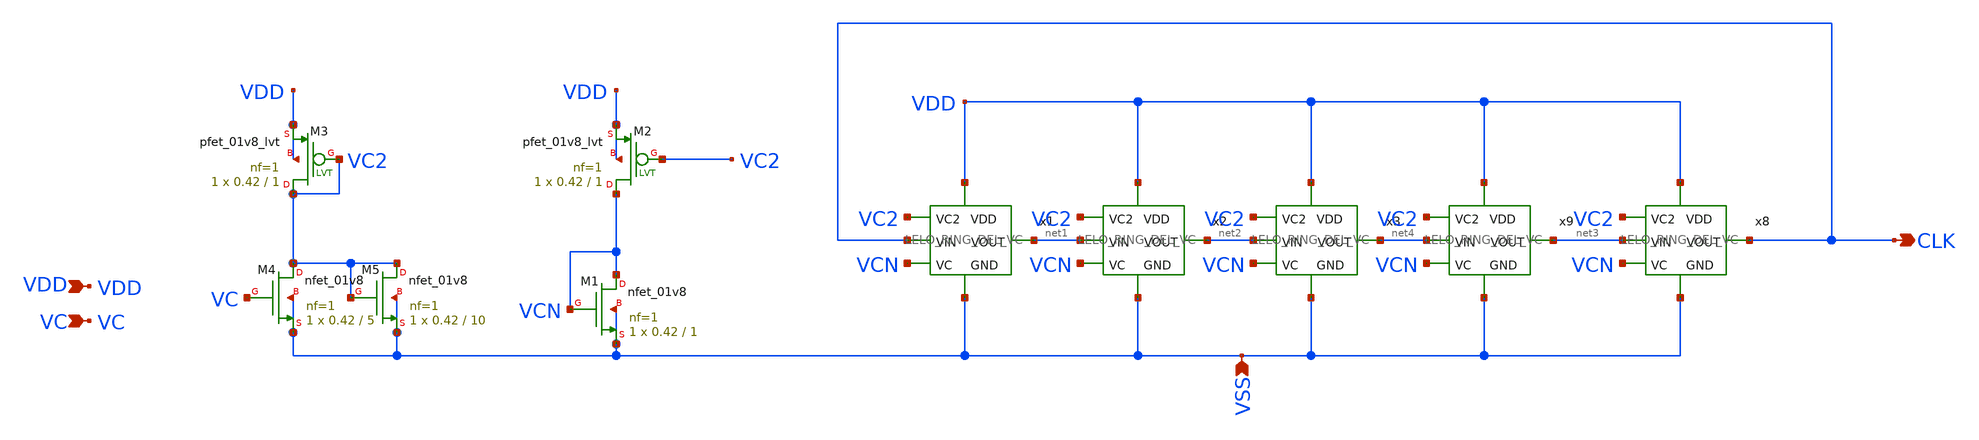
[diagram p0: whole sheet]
** sch_path: design/LELO_SVOD_SKY130A/RO.sch
**.subckt RO CLK VSS VDD VC
*.opin CLK
*.ipin VSS
*.ipin VDD
*.ipin VC
x1 VDD VC2 CLK net1 VCN VSS LELO_RING_DEL_VC
x2 VDD VC2 net1 net2 VCN VSS LELO_RING_DEL_VC
x3 VDD VC2 net2 net4 VCN VSS LELO_RING_DEL_VC
XM1 VCN VCN VSS VSS sky130_fd_pr__nfet_01v8 L=1 W=0.42 nf=1 ad='int((1 + 1)/2) * 0.42 / 1 * 0.29' as='int((1 + 2)/2) * 0.42 / 1 * 0.29'
+ pd='2*int((1 + 1)/2) * (0.42 / 1 + 0.29)' ps='2*int((1 + 2)/2) * (0.42 / 1 + 0.29)' nrd='0.29 / 0.42 '
+ nrs='0.29 / 0.42 ' sa=0 sb=0 sd=0 mult=1 m=1
XM4 VC2 VC VSS VSS sky130_fd_pr__nfet_01v8 L=5 W=0.42 nf=1 ad='int((1 + 1)/2) * 0.42 / 1 * 0.29' as='int((1 + 2)/2) * 0.42 / 1 * 0.29'
+ pd='2*int((1 + 1)/2) * (0.42 / 1 + 0.29)' ps='2*int((1 + 2)/2) * (0.42 / 1 + 0.29)' nrd='0.29 / 0.42 '
+ nrs='0.29 / 0.42 ' sa=0 sb=0 sd=0 mult=1 m=1
XM2 VCN VC2 VDD VDD sky130_fd_pr__pfet_01v8_lvt L=1 W=0.42 nf=1 ad='int((1 + 1)/2) * 0.42 / 1 * 0.29'
+ as='int((1 + 2)/2) * 0.42 / 1 * 0.29' pd='2*int((1 + 1)/2) * (0.42 / 1 + 0.29)' ps='2*int((1 + 2)/2) * (0.42 / 1 + 0.29)'
+ nrd='0.29 / 0.42 ' nrs='0.29 / 0.42 ' sa=0 sb=0 sd=0 mult=1 m=1
XM3 VC2 VC2 VDD VDD sky130_fd_pr__pfet_01v8_lvt L=1 W=0.42 nf=1 ad='int((1 + 1)/2) * 0.42 / 1 * 0.29'
+ as='int((1 + 2)/2) * 0.42 / 1 * 0.29' pd='2*int((1 + 1)/2) * (0.42 / 1 + 0.29)' ps='2*int((1 + 2)/2) * (0.42 / 1 + 0.29)'
+ nrd='0.29 / 0.42 ' nrs='0.29 / 0.42 ' sa=0 sb=0 sd=0 mult=1 m=1
XM5 VC2 VC2 VSS VSS sky130_fd_pr__nfet_01v8 L=10 W=0.42 nf=1 ad='int((1 + 1)/2) * 0.42 / 1 * 0.29' as='int((1 + 2)/2) * 0.42 / 1 * 0.29'
+ pd='2*int((1 + 1)/2) * (0.42 / 1 + 0.29)' ps='2*int((1 + 2)/2) * (0.42 / 1 + 0.29)' nrd='0.29 / 0.42 '
+ nrs='0.29 / 0.42 ' sa=0 sb=0 sd=0 mult=1 m=1
x8 VDD VC2 net3 CLK VCN VSS LELO_RING_DEL_VC
x9 VDD VC2 net4 net3 VCN VSS LELO_RING_DEL_VC
**.ends

* expanding   symbol:  LELO_SVOD_SKY130A/LELO_RING_DEL_VC.sym # of pins=6
** sym_path: design/LELO_SVOD_SKY130A/LELO_RING_DEL_VC.sym
** sch_path: design/LELO_SVOD_SKY130A/LELO_RING_DEL_VC.sch
.subckt LELO_RING_DEL_VC VDD VC2 VIN VOUT VC GND
*.ipin VIN
*.ipin VDD
*.ipin GND
*.opin VOUT
*.ipin VC
*.ipin VC2
XM3 VOUT VIN net1 GND sky130_fd_pr__nfet_01v8 L=1 W=0.42 nf=1 ad='int((1 + 1)/2) * 0.42 / 1 * 0.29' as='int((1 + 2)/2) * 0.42 / 1 * 0.29'
+ pd='2*int((1 + 1)/2) * (0.42 / 1 + 0.29)' ps='2*int((1 + 2)/2) * (0.42 / 1 + 0.29)' nrd='0.29 / 0.42 '
+ nrs='0.29 / 0.42 ' sa=0 sb=0 sd=0 mult=1 m=1
XM4 net1 VC GND GND sky130_fd_pr__nfet_01v8 L=4 W=0.42 nf=1 ad='int((1 + 1)/2) * 0.42 / 1 * 0.29' as='int((1 + 2)/2) * 0.42 / 1 * 0.29'
+ pd='2*int((1 + 1)/2) * (0.42 / 1 + 0.29)' ps='2*int((1 + 2)/2) * (0.42 / 1 + 0.29)' nrd='0.29 / 0.42 '
+ nrs='0.29 / 0.42 ' sa=0 sb=0 sd=0 mult=1 m=1
XM1 net2 VC2 VDD VDD sky130_fd_pr__pfet_01v8_lvt L=4 W=0.42 nf=1 ad='int((1 + 1)/2) * 0.42 / 1 * 0.29'
+ as='int((1 + 2)/2) * 0.42 / 1 * 0.29' pd='2*int((1 + 1)/2) * (0.42 / 1 + 0.29)' ps='2*int((1 + 2)/2) * (0.42 / 1 + 0.29)'
+ nrd='0.29 / 0.42 ' nrs='0.29 / 0.42 ' sa=0 sb=0 sd=0 mult=1 m=1
XM2 VOUT VIN net2 VDD sky130_fd_pr__pfet_01v8_lvt L=0.35 W=1 nf=1 ad='int((1 + 1)/2) * 1 / 1 * 0.29'
+ as='int((1 + 2)/2) * 1 / 1 * 0.29' pd='2*int((1 + 1)/2) * (1 / 1 + 0.29)' ps='2*int((1 + 2)/2) * (1 / 1 + 0.29)'
+ nrd='0.29 / 1 ' nrs='0.29 / 1 ' sa=0 sb=0 sd=0 mult=1 m=1
.ends

.end
